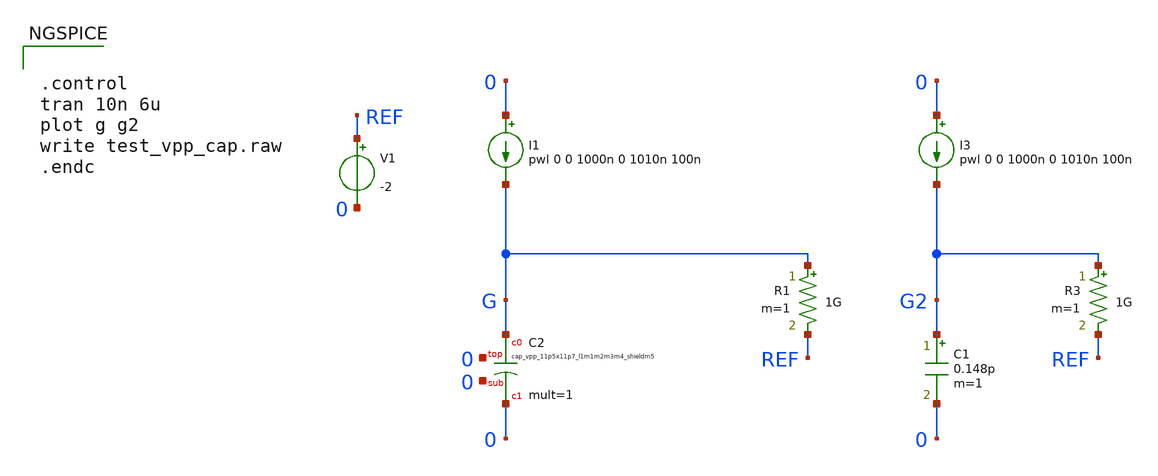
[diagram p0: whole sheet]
** sch_path: xyce/sky130A-xyce/libs.tech/xschem/sky130_tests/test_vpp_cap.sch
* Copyright 2020 Stefan Frederik Schippers
* Licensed under the Apache License, Version 2.0 (the "License");
* you may not use this file except in compliance with the License.
* You may obtain a copy of the License at
* https://www.apache.org/licenses/LICENSE-2.0
* Unless required by applicable law or agreed to in writing, software
* distributed under the License is distributed on an "AS IS" BASIS,
* WITHOUT WARRANTIES OR CONDITIONS OF ANY KIND, either express or implied.
* See the License for the specific language governing permissions and
* limitations under the License.
**.subckt test_vpp_cap
I1 0 G pwl 0 0 1000n 0 1010n 100n
R1 G REF 1G m=1
I3 0 G2 pwl 0 0 1000n 0 1010n 100n
R3 G2 REF 1G m=1
C1 G2 0 0.148p m=1
V1 REF 0 -2
XC2 G 0 0 0 sky130_fd_pr__cap_vpp_11p5x11p7_l1m1m2m3m4_shieldm5 W=1 L=1 mult=1 m=1
**** begin user architecture code


.control
tran 10n 6u
plot g g2
write test_vpp_cap.raw
.endc



.include $::SKYWATER_MODELS/cells/nfet_01v8/sky130_fd_pr__nfet_01v8__tt.corner.spice
.include $::SKYWATER_MODELS/cells/nfet_01v8_lvt/sky130_fd_pr__nfet_01v8_lvt__tt.corner.spice
.include $::SKYWATER_MODELS/cells/pfet_01v8/sky130_fd_pr__pfet_01v8__tt.corner.spice
.include $::SKYWATER_MODELS/cells/nfet_03v3_nvt/sky130_fd_pr__nfet_03v3_nvt__tt.corner.spice
.include $::SKYWATER_MODELS/cells/nfet_05v0_nvt/sky130_fd_pr__nfet_05v0_nvt__tt.corner.spice
.include $::SKYWATER_MODELS/cells/esd_nfet_01v8/sky130_fd_pr__esd_nfet_01v8__tt.corner.spice
.include $::SKYWATER_MODELS/cells/pfet_01v8_lvt/sky130_fd_pr__pfet_01v8_lvt__tt.corner.spice
.include $::SKYWATER_MODELS/cells/pfet_01v8_hvt/sky130_fd_pr__pfet_01v8_hvt__tt.corner.spice
.include $::SKYWATER_MODELS/cells/esd_pfet_g5v0d10v5/sky130_fd_pr__esd_pfet_g5v0d10v5__tt.corner.spice
.include $::SKYWATER_MODELS/cells/pfet_g5v0d10v5/sky130_fd_pr__pfet_g5v0d10v5__tt.corner.spice
.include $::SKYWATER_MODELS/cells/pfet_g5v0d16v0/sky130_fd_pr__pfet_g5v0d16v0__tt.corner.spice
.include $::SKYWATER_MODELS/cells/nfet_g5v0d10v5/sky130_fd_pr__nfet_g5v0d10v5__tt.corner.spice
.include $::SKYWATER_MODELS/cells/nfet_g5v0d16v0/sky130_fd_pr__nfet_g5v0d16v0__tt_discrete.corner.spice
.include $::SKYWATER_MODELS/cells/esd_nfet_g5v0d10v5/sky130_fd_pr__esd_nfet_g5v0d10v5__tt.corner.spice
.include $::SKYWATER_MODELS/models/corners/tt/nonfet.spice
* Mismatch parameters
.include $::SKYWATER_MODELS/cells/nfet_01v8/sky130_fd_pr__nfet_01v8__mismatch.corner.spice
.include $::SKYWATER_MODELS/cells/pfet_01v8/sky130_fd_pr__pfet_01v8__mismatch.corner.spice
.include $::SKYWATER_MODELS/cells/nfet_01v8_lvt/sky130_fd_pr__nfet_01v8_lvt__mismatch.corner.spice
.include $::SKYWATER_MODELS/cells/pfet_01v8_lvt/sky130_fd_pr__pfet_01v8_lvt__mismatch.corner.spice
.include $::SKYWATER_MODELS/cells/pfet_01v8_hvt/sky130_fd_pr__pfet_01v8_hvt__mismatch.corner.spice
.include $::SKYWATER_MODELS/cells/nfet_g5v0d10v5/sky130_fd_pr__nfet_g5v0d10v5__mismatch.corner.spice
.include $::SKYWATER_MODELS/cells/pfet_g5v0d10v5/sky130_fd_pr__pfet_g5v0d10v5__mismatch.corner.spice
.include $::SKYWATER_MODELS/cells/nfet_05v0_nvt/sky130_fd_pr__nfet_05v0_nvt__mismatch.corner.spice
.include $::SKYWATER_MODELS/cells/nfet_03v3_nvt/sky130_fd_pr__nfet_03v3_nvt__mismatch.corner.spice
* Resistor$::SKYWATER_MODELS/Capacitor
.include $::SKYWATER_MODELS/models/r+c/res_typical__cap_typical.spice
.include $::SKYWATER_MODELS/models/r+c/res_typical__cap_typical__lin.spice
* Special cells
.include $::SKYWATER_MODELS/models/corners/tt/specialized_cells.spice
* All models
.include $::SKYWATER_MODELS/models/all.spice
* Corner
.include $::SKYWATER_MODELS/models/corners/tt/rf.spice

**** end user architecture code
**.ends
.end
